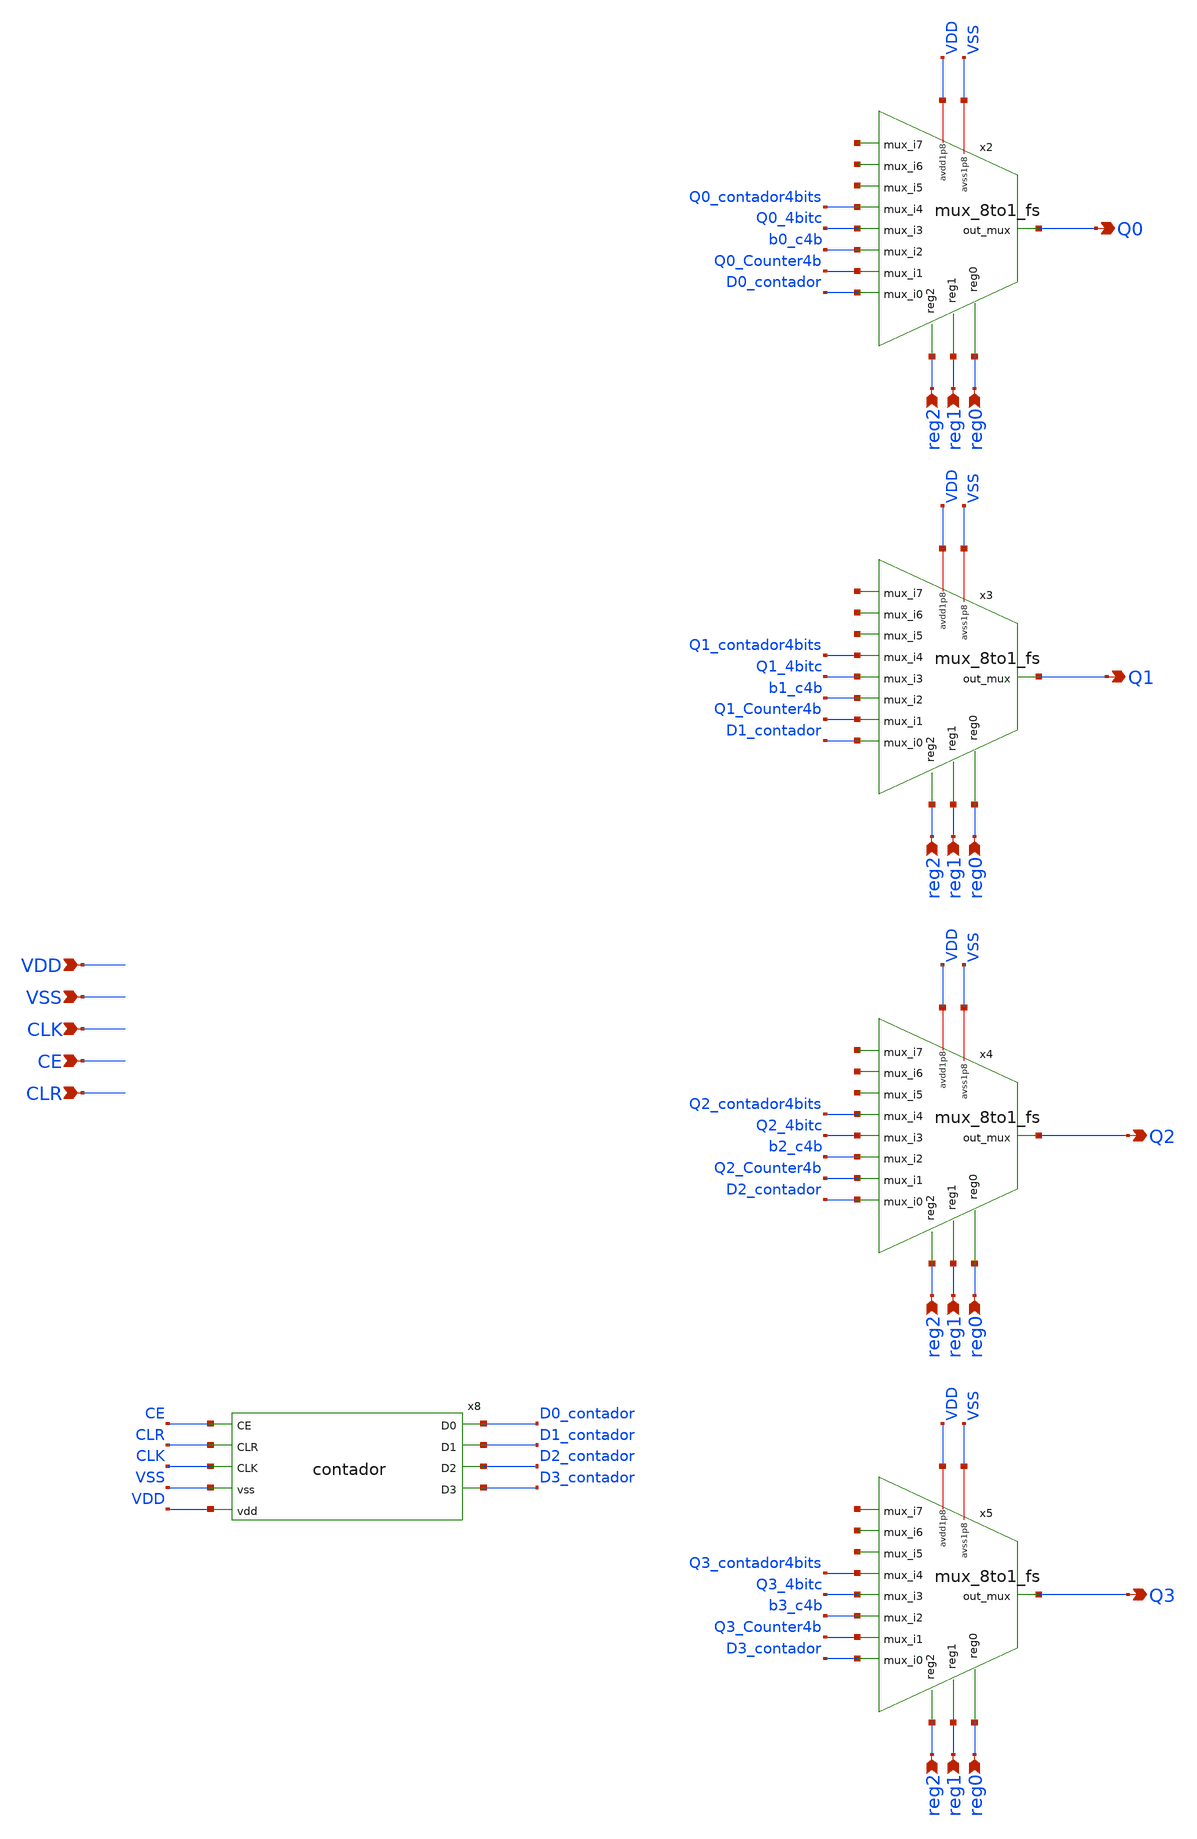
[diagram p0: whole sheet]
** sch_path: track_vlsi/toplevel_vlsi/sch/toplevel_parcial.sch
**.subckt toplevel_parcial VDD VSS CLK CE CLR reg2 reg1 reg0 reg2 reg1 reg0 reg2 reg1 reg0 Q0 Q1 Q2
*+ Q3 reg2 reg1 reg0
*.ipin VDD
*.ipin VSS
*.ipin CLK
*.ipin CE
*.ipin CLR
*.ipin reg2
*.ipin reg1
*.ipin reg0
*.ipin reg2
*.ipin reg1
*.ipin reg0
*.ipin reg2
*.ipin reg1
*.ipin reg0
*.opin Q0
*.opin Q1
*.opin Q2
*.opin Q3
*.ipin reg2
*.ipin reg1
*.ipin reg0
x2 VDD VSS net1 net2 net3 Q0 Q0_contador4bits Q0_4bitc reg0 b0_c4b Q0_Counter4b D0_contador reg1
+ reg2 mux_8to1_fs
x3 VDD VSS net4 net5 net6 Q1 Q1_contador4bits Q1_4bitc reg0 b1_c4b Q1_Counter4b D1_contador reg1
+ reg2 mux_8to1_fs
x4 VDD VSS net7 net8 net9 Q2 Q2_contador4bits Q2_4bitc reg0 b2_c4b Q2_Counter4b D2_contador reg1
+ reg2 mux_8to1_fs
x5 VDD VSS net10 net11 net12 Q3 Q3_contador4bits Q3_4bitc reg0 b3_c4b Q3_Counter4b D3_contador reg1
+ reg2 mux_8to1_fs
x8 D0_contador CE CLR CLK VSS VDD D1_contador D2_contador D3_contador contador
**.ends
.end
